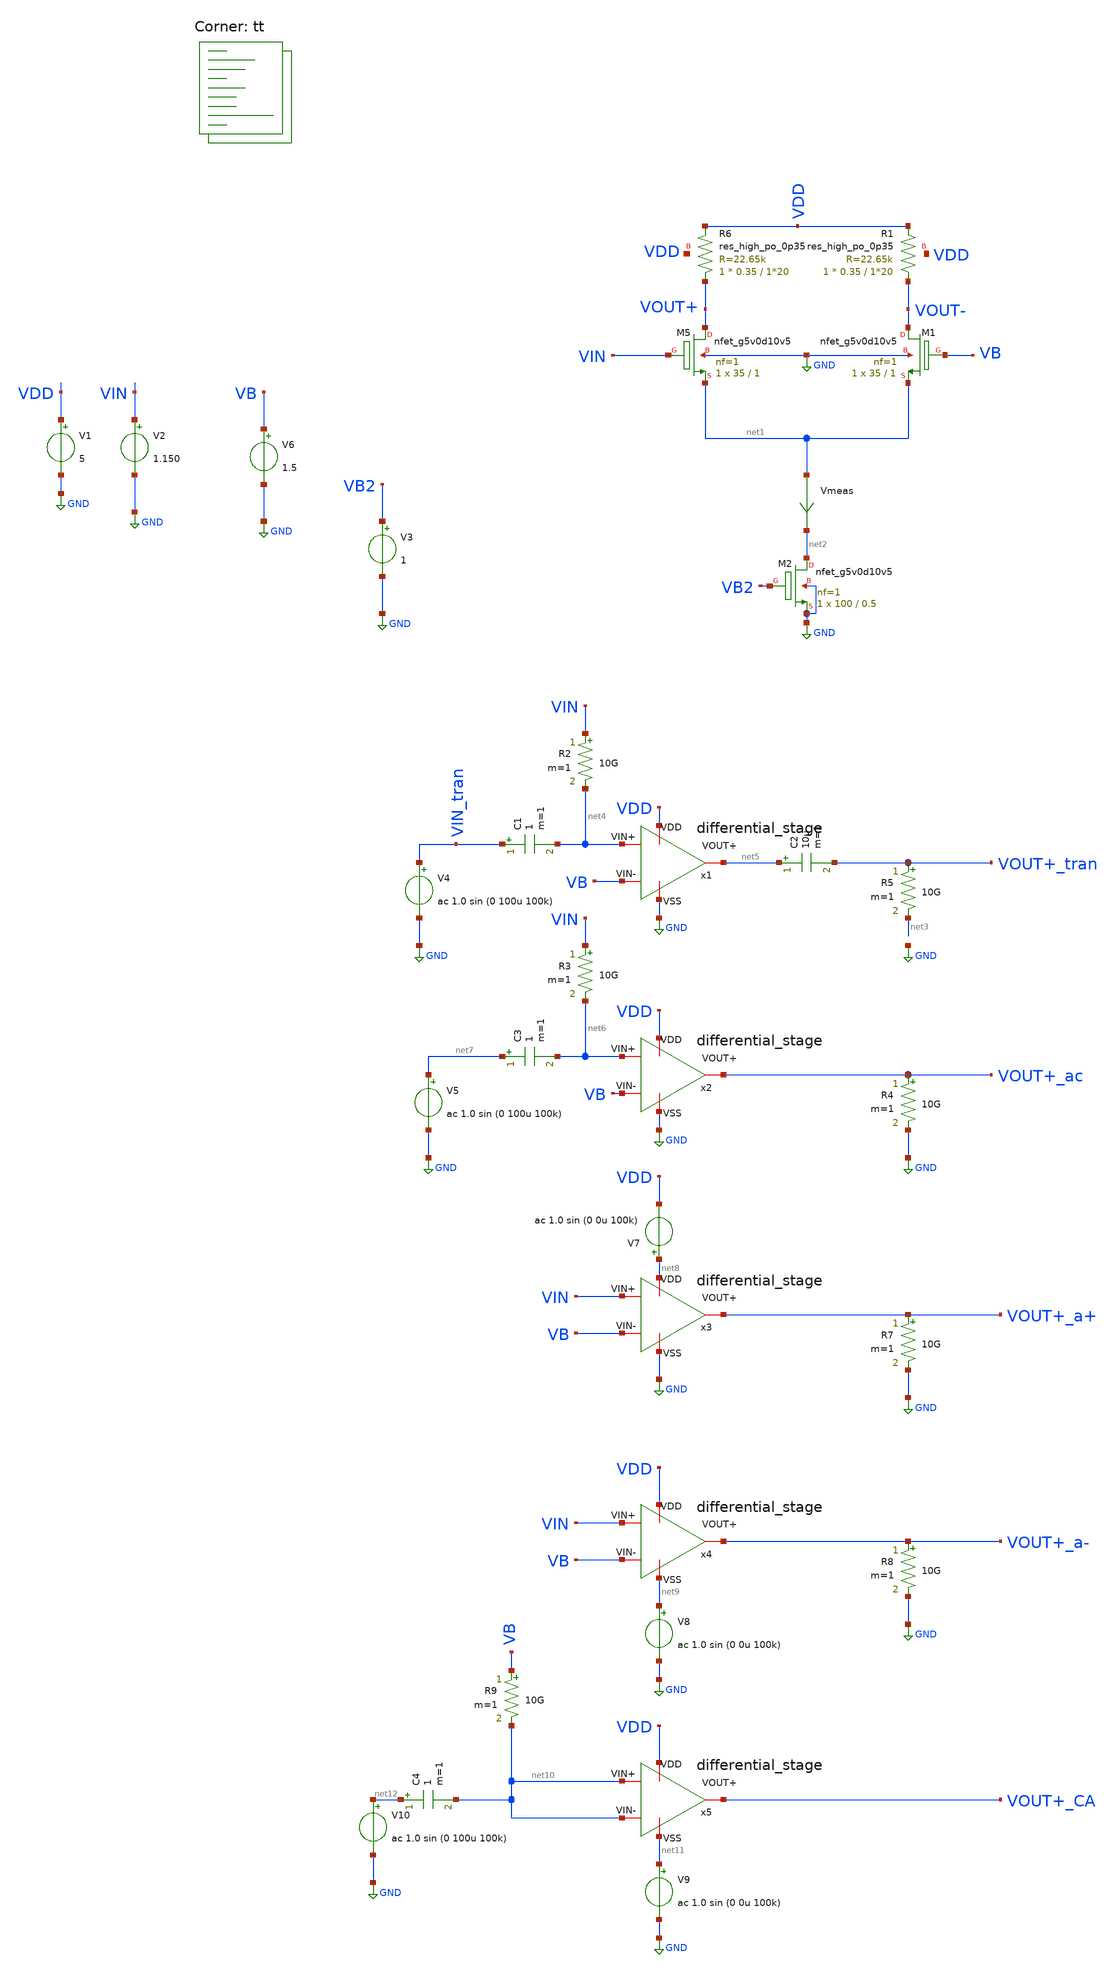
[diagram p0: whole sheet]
** sch_path: amplifiers/differencial_stage_amps/basic_stages/basic_stage/diferential_stage.sch
**.subckt diferential_stage
XM5 VOUT+ VIN net1 GND sky130_fd_pr__nfet_g5v0d10v5 L=1 W=35 nf=1 ad='int((1 + 1)/2) * 35 / 1 * 0.29'
+ as='int((1 + 2)/2) * 35 / 1 * 0.29' pd='2*int((1 + 1)/2) * (35 / 1 + 0.29)' ps='2*int((1 + 2)/2) * (35 / 1 + 0.29)'
+ nrd='0.29 / 35 ' nrs='0.29 / 35 ' sa=0 sb=0 sd=0 mult=1 m=1
XM1 VOUT- VB net1 GND sky130_fd_pr__nfet_g5v0d10v5 L=1 W=35 nf=1 ad='int((1 + 1)/2) * 35 / 1 * 0.29'
+ as='int((1 + 2)/2) * 35 / 1 * 0.29' pd='2*int((1 + 1)/2) * (35 / 1 + 0.29)' ps='2*int((1 + 2)/2) * (35 / 1 + 0.29)'
+ nrd='0.29 / 35 ' nrs='0.29 / 35 ' sa=0 sb=0 sd=0 mult=1 m=1
XR6 VOUT+ VDD VDD sky130_fd_pr__res_high_po_0p35 L=1*20 mult=1 m=1
XR1 VOUT- VDD VDD sky130_fd_pr__res_high_po_0p35 L=1*20 mult=1 m=1
V1 VDD GND 5
V2 VIN GND 1.150
V6 VB GND 1.5
XM2 net2 VB2 GND GND sky130_fd_pr__nfet_g5v0d10v5 L=0.5 W=100 nf=1 ad='int((1 + 1)/2) * 100 / 1 * 0.29'
+ as='int((1 + 2)/2) * 100 / 1 * 0.29' pd='2*int((1 + 1)/2) * (100 / 1 + 0.29)' ps='2*int((1 + 2)/2) * (100 / 1 + 0.29)'
+ nrd='0.29 / 100 ' nrs='0.29 / 100 ' sa=0 sb=0 sd=0 mult=1 m=1
V3 VB2 GND 1
Vmeas net1 net2 0
.save i(vmeas)
x1 VDD GND net4 VB net5 differential_stage
R5 VOUT+_tran net3 10G m=1
R2 VIN net4 10G m=1
V4 VIN_tran GND ac 1.0 sin (0 100u 100k)
C2 net5 VOUT+_tran 10u m=1
C1 VIN_tran net4 1 m=1
x2 VDD GND net6 VB VOUT+_ac differential_stage
R3 VIN net6 10G m=1
C3 net7 net6 1 m=1
V5 net7 GND ac 1.0 sin (0 100u 100k)
R4 VOUT+_ac GND 10G m=1
x3 net8 GND VIN VB VOUT+_a+ differential_stage
V7 net8 VDD ac 1.0 sin (0 0u 100k)
R7 VOUT+_a+ GND 10G m=1
x4 VDD net9 VIN VB VOUT+_a- differential_stage
V8 net9 GND ac 1.0 sin (0 0u 100k)
R8 VOUT+_a- GND 10G m=1
x5 VDD net11 net10 net10 VOUT+_CA differential_stage
V9 net11 GND ac 1.0 sin (0 0u 100k)
R9 VB net10 10G m=1
C4 net12 net10 1 m=1
V10 net12 GND ac 1.0 sin (0 100u 100k)
**** begin user architecture code

**************************************************************
**************************************************************
**************************************************************
**************************************************************
**************************************************************
*LIBs*********************************************************
**************************************************************
**************************************************************
**************************************************************
**************************************************************
**************************************************************
*.lib $::SKYWATER_MODELS/sky130.lib.spice tt
* chose the corners in the corner file
* tt_mm for mismatch
* ss ff sf fs standart corners
* ll hh lh hl capacitor and resistors corners
* mc for total process variation including corners
**************************************************************
**************************************************************
**************************************************************
**************************************************************
**************************************************************
*Corners/montecarlo options***********************************
**************************************************************
**************************************************************
**************************************************************
**************************************************************
**************************************************************
.TEMP 27
**************************************************************
**************************************************************
**************************************************************
**************************************************************
*SIMULATION and Plots*****************************************
**************************************************************
**************************************************************
**************************************************************
**************************************************************
.control
save all
dc V2 0 5 0.01
*dc simulation
plot v(VOUT-) v(VIN) deriv(v(VOUT-)) v(VOUT+) deriv(v(VOUT+))
*ploting VIN VOUT and the voltage gain
plot i(Vmeas)
*ploting the current for curiosity
tran 0.05ns 20u
*transient simulation
plot (v(VOUT+_tran)) v(VIN_tran)
*simple plot to exemplify the gain
fft v(VOUT+_tran) v(VIN_tran)
*fast fourier transfor
plot mag(v(VOUT+_tran)) mag(v(VIN_tran))
ac dec 20 1 1000G
*simple ac simulation
plot db(v(VOUT+_ac))
plot db(v(VOUT+_a+))
plot db(v(VOUT+_a-))
plot db(v(VOUT+_CA))
plot db((v(VOUT+_ac))/(v(VOUT+_CA)))
plot db((v(VOUT+_ac))/(v(VOUT+_a+)))
plot db((v(VOUT+_ac))/(v(VOUT+_a-)))
.endc

.lib $::SKYWATER_MODELS/sky130.lib.spice tt
**** end user architecture code
**.ends
.GLOBAL GND
.end
